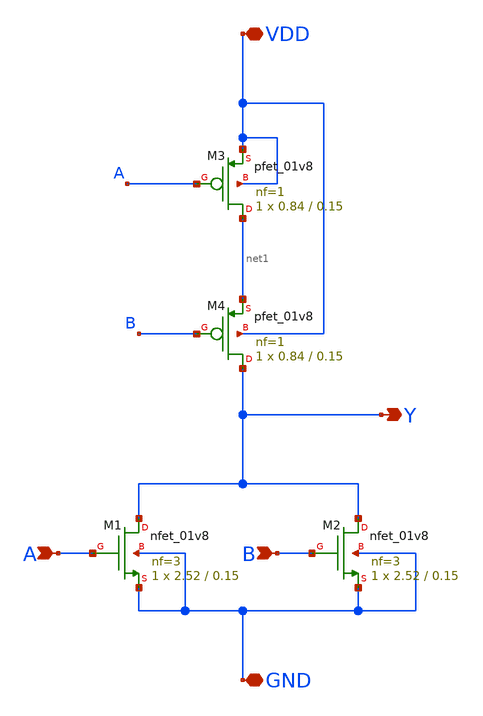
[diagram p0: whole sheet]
** sch_path: cells/NOR2X1/schematic/nor2x1.sch
**.subckt nor2x1 A B VDD GND Y
*.ipin A
*.ipin B
*.iopin VDD
*.iopin GND
*.opin Y
XM1 Y A GND GND sky130_fd_pr__nfet_01v8 L=0.15 W=2.52 nf=3 ad='int((3 + 1)/2) * 2.52 / 3 * 0.29' as='int((3 + 2)/2) * 2.52 / 3 * 0.29'
+ pd='2*int((3 + 1)/2) * (2.52 / 3 + 0.29)' ps='2*int((3 + 2)/2) * (2.52 / 3 + 0.29)' nrd='0.29 / 2.52 '
+ nrs='0.29 / 2.52 ' sa=0 sb=0 sd=0 mult=1 m=1
XM3 net1 A VDD VDD sky130_fd_pr__pfet_01v8 L=0.15 W=0.84 nf=1 ad='int((1 + 1)/2) * 0.84 / 1 * 0.29' as='int((1 + 2)/2) * 0.84 / 1 * 0.29'
+ pd='2*int((1 + 1)/2) * (0.84 / 1 + 0.29)' ps='2*int((1 + 2)/2) * (0.84 / 1 + 0.29)' nrd='0.29 / 0.84 '
+ nrs='0.29 / 0.84 ' sa=0 sb=0 sd=0 mult=1 m=1
XM4 Y B net1 VDD sky130_fd_pr__pfet_01v8 L=0.15 W=0.84 nf=1 ad='int((1 + 1)/2) * 0.84 / 1 * 0.29' as='int((1 + 2)/2) * 0.84 / 1 * 0.29'
+ pd='2*int((1 + 1)/2) * (0.84 / 1 + 0.29)' ps='2*int((1 + 2)/2) * (0.84 / 1 + 0.29)' nrd='0.29 / 0.84 '
+ nrs='0.29 / 0.84 ' sa=0 sb=0 sd=0 mult=1 m=1
XM2 Y B GND GND sky130_fd_pr__nfet_01v8 L=0.15 W=2.52 nf=3 ad='int((3 + 1)/2) * 2.52 / 3 * 0.29' as='int((3 + 2)/2) * 2.52 / 3 * 0.29'
+ pd='2*int((3 + 1)/2) * (2.52 / 3 + 0.29)' ps='2*int((3 + 2)/2) * (2.52 / 3 + 0.29)' nrd='0.29 / 2.52 '
+ nrs='0.29 / 2.52 ' sa=0 sb=0 sd=0 mult=1 m=1
**.ends
.end
